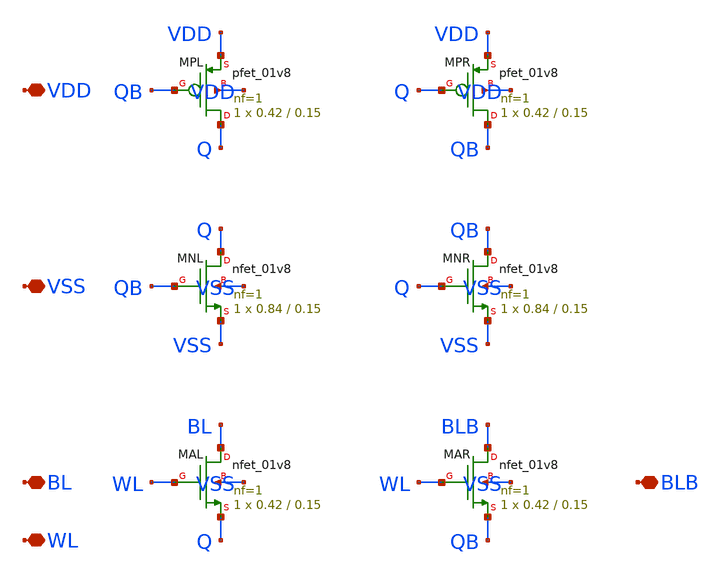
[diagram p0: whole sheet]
** sch_path: design/bitcell/bitcell_6t.sch
**.subckt bitcell_6t BL BLB WL VDD VSS
*.iopin BL
*.iopin BLB
*.iopin WL
*.iopin VDD
*.iopin VSS
XMPL Q QB VDD VDD sky130_fd_pr__pfet_01v8 L=0.15 W=0.42 nf=1 ad=0.1218 as=0.1218 pd=1.42 ps=1.42
+ nrd=0.6905 nrs=0.6905 sa=0 sb=0 sd=0 mult=1 m=1
XMPR QB Q VDD VDD sky130_fd_pr__pfet_01v8 L=0.15 W=0.42 nf=1 ad=0.1218 as=0.1218 pd=1.42 ps=1.42
+ nrd=0.6905 nrs=0.6905 sa=0 sb=0 sd=0 mult=1 m=1
XMNL Q QB VSS VSS sky130_fd_pr__nfet_01v8 L=0.15 W=0.84 nf=1 ad=0.2436 as=0.2436 pd=2.26 ps=2.26
+ nrd=0.3452 nrs=0.3452 sa=0 sb=0 sd=0 mult=1 m=1
XMNR QB Q VSS VSS sky130_fd_pr__nfet_01v8 L=0.15 W=0.84 nf=1 ad=0.2436 as=0.2436 pd=2.26 ps=2.26
+ nrd=0.3452 nrs=0.3452 sa=0 sb=0 sd=0 mult=1 m=1
XMAL BL WL Q VSS sky130_fd_pr__nfet_01v8 L=0.15 W=0.42 nf=1 ad=0.1218 as=0.1218 pd=1.42 ps=1.42
+ nrd=0.6905 nrs=0.6905 sa=0 sb=0 sd=0 mult=1 m=1
XMAR BLB WL QB VSS sky130_fd_pr__nfet_01v8 L=0.15 W=0.42 nf=1 ad=0.1218 as=0.1218 pd=1.42 ps=1.42
+ nrd=0.6905 nrs=0.6905 sa=0 sb=0 sd=0 mult=1 m=1
**.ends
.end
